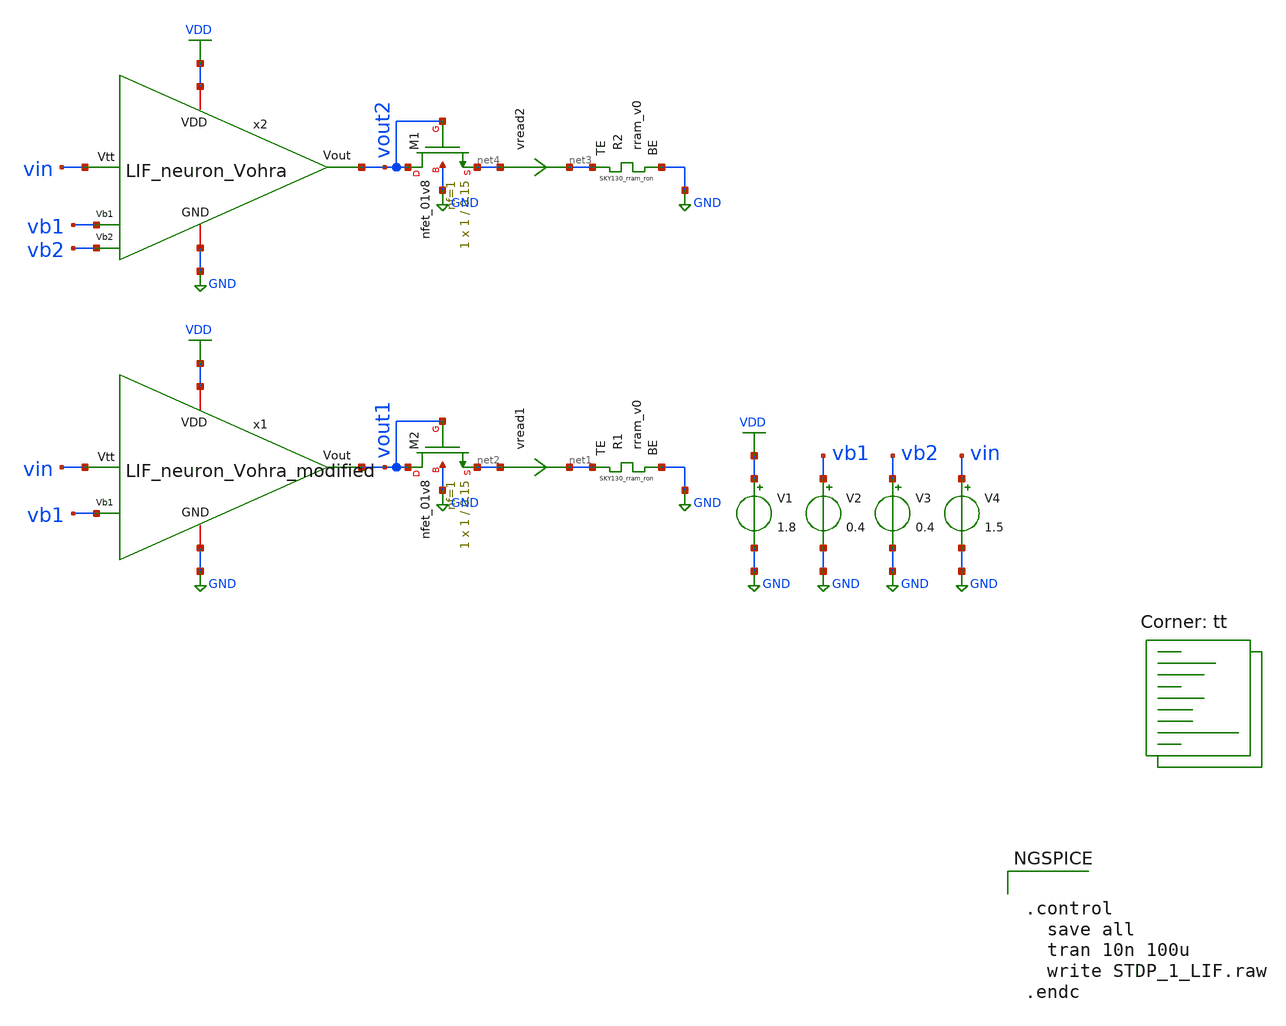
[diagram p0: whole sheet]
** sch_path: STDP/STDP_1_LIF_modified.sch
**.subckt STDP_1_LIF_modified
V1 VDD GND 1.8
V4 vin GND 1.5
V2 vb1 GND 0.4
XR1 net1 GND rram_v0
vread1 net2 net1 0
.save i(vread1)
x1 VDD vout1 vb1 GND vin LIF_neuron_Vohra_modified
x2 VDD vout2 vb1 vin GND vb2 LIF_neuron_Vohra
V3 vb2 GND 0.4
XR2 net3 GND rram_v0
vread2 net4 net3 0
.save i(vread2)
XM1 vout2 vout2 net4 GND sky130_fd_pr__nfet_01v8 L=0.15 W=1 nf=1 ad='int((nf+1)/2) * W/nf * 0.29' as='int((nf+2)/2) * W/nf * 0.29'
+ pd='2*int((nf+1)/2) * (W/nf + 0.29)' ps='2*int((nf+2)/2) * (W/nf + 0.29)' nrd='0.29 / W' nrs='0.29 / W'
+ sa=0 sb=0 sd=0 mult=1 m=1
XM2 vout1 vout1 net2 GND sky130_fd_pr__nfet_01v8 L=0.15 W=1 nf=1 ad='int((nf+1)/2) * W/nf * 0.29' as='int((nf+2)/2) * W/nf * 0.29'
+ pd='2*int((nf+1)/2) * (W/nf + 0.29)' ps='2*int((nf+2)/2) * (W/nf + 0.29)' nrd='0.29 / W' nrs='0.29 / W'
+ sa=0 sb=0 sd=0 mult=1 m=1
**** begin user architecture code
.lib $::SKYWATER_MODELS/sky130.lib.spice tt

** opencircuitdesign pdks install
.inc $::SKYWATER_MODELS/rram_v0.spice



.control
  save all
  tran 10n 100u
  write STDP_1_LIF.raw
.endc


**** end user architecture code
**.ends

* expanding   symbol:
*+  /home/ricardo/RATT_repos/Proyectos_xschem/LIF_neuron/LIF_neuron_Vohra_modified.sym # of pins=5
** sym_path: LIF_neuron/LIF_neuron_Vohra_modified.sym
** sch_path: LIF_neuron/LIF_neuron_Vohra_modified.sch
.subckt LIF_neuron_Vohra_modified VDD Vout Vb1 GND Vtt
*.ipin Vtt
*.iopin GND
*.ipin Vb1
*.iopin VDD
*.opin Vout
XM1 net2 Vtt GND GND sky130_fd_pr__nfet_01v8 L=1 W=0.6 nf=1 ad='int((nf+1)/2) * W/nf * 0.29' as='int((nf+2)/2) * W/nf * 0.29'
+ pd='2*int((nf+1)/2) * (W/nf + 0.29)' ps='2*int((nf+2)/2) * (W/nf + 0.29)' nrd='0.29 / W' nrs='0.29 / W'
+ sa=0 sb=0 sd=0 mult=1 m=1
XM3 net2 net2 VDD VDD sky130_fd_pr__pfet_01v8 L=1 W=0.6 nf=1 ad='int((nf+1)/2) * W/nf * 0.29' as='int((nf+2)/2) * W/nf * 0.29'
+ pd='2*int((nf+1)/2) * (W/nf + 0.29)' ps='2*int((nf+2)/2) * (W/nf + 0.29)' nrd='0.29 / W' nrs='0.29 / W'
+ sa=0 sb=0 sd=0 mult=1 m=1
XM13 net4 Vb1 GND GND sky130_fd_pr__nfet_01v8 L=0.5 W=5 nf=1 ad='int((nf+1)/2) * W/nf * 0.29' as='int((nf+2)/2) * W/nf * 0.29'
+ pd='2*int((nf+1)/2) * (W/nf + 0.29)' ps='2*int((nf+2)/2) * (W/nf + 0.29)' nrd='0.29 / W' nrs='0.29 / W'
+ sa=0 sb=0 sd=0 mult=1 m=1
XM12 rc net1 net5 GND sky130_fd_pr__nfet_01v8 L=1 W=1 nf=1 ad='int((nf+1)/2) * W/nf * 0.29' as='int((nf+2)/2) * W/nf * 0.29'
+ pd='2*int((nf+1)/2) * (W/nf + 0.29)' ps='2*int((nf+2)/2) * (W/nf + 0.29)' nrd='0.29 / W' nrs='0.29 / W'
+ sa=0 sb=0 sd=0 mult=1 m=1
XM11 rc net1 VDD VDD sky130_fd_pr__pfet_01v8 L=1 W=1 nf=1 ad='int((nf+1)/2) * W/nf * 0.29' as='int((nf+2)/2) * W/nf * 0.29'
+ pd='2*int((nf+1)/2) * (W/nf + 0.29)' ps='2*int((nf+2)/2) * (W/nf + 0.29)' nrd='0.29 / W' nrs='0.29 / W'
+ sa=0 sb=0 sd=0 mult=1 m=1
XC1 rc GND sky130_fd_pr__cap_mim_m3_1 W=21 L=1 MF=1 m=1
XM14 u rc GND GND sky130_fd_pr__nfet_01v8 L=4 W=1 nf=1 ad='int((nf+1)/2) * W/nf * 0.29' as='int((nf+2)/2) * W/nf * 0.29'
+ pd='2*int((nf+1)/2) * (W/nf + 0.29)' ps='2*int((nf+2)/2) * (W/nf + 0.29)' nrd='0.29 / W' nrs='0.29 / W'
+ sa=0 sb=0 sd=0 mult=1 m=1
XM4 u net2 VDD VDD sky130_fd_pr__pfet_01v8 L=1 W=1 nf=1 ad='int((nf+1)/2) * W/nf * 0.29' as='int((nf+2)/2) * W/nf * 0.29'
+ pd='2*int((nf+1)/2) * (W/nf + 0.29)' ps='2*int((nf+2)/2) * (W/nf + 0.29)' nrd='0.29 / W' nrs='0.29 / W'
+ sa=0 sb=0 sd=0 mult=1 m=1
XC2 u GND sky130_fd_pr__cap_mim_m3_1 W=10 L=1 MF=50 m=50
XM6 net3 Vout GND GND sky130_fd_pr__nfet_01v8 L=0.5 W=1 nf=1 ad='int((nf+1)/2) * W/nf * 0.29' as='int((nf+2)/2) * W/nf * 0.29'
+ pd='2*int((nf+1)/2) * (W/nf + 0.29)' ps='2*int((nf+2)/2) * (W/nf + 0.29)' nrd='0.29 / W' nrs='0.29 / W'
+ sa=0 sb=0 sd=0 mult=1 m=1
XM7 net1 u net3 GND sky130_fd_pr__nfet_01v8 L=1 W=1 nf=1 ad='int((nf+1)/2) * W/nf * 0.29' as='int((nf+2)/2) * W/nf * 0.29'
+ pd='2*int((nf+1)/2) * (W/nf + 0.29)' ps='2*int((nf+2)/2) * (W/nf + 0.29)' nrd='0.29 / W' nrs='0.29 / W'
+ sa=0 sb=0 sd=0 mult=1 m=1
XM8 net1 u VDD VDD sky130_fd_pr__pfet_01v8 L=1 W=1 nf=1 ad='int((nf+1)/2) * W/nf * 0.29' as='int((nf+2)/2) * W/nf * 0.29'
+ pd='2*int((nf+1)/2) * (W/nf + 0.29)' ps='2*int((nf+2)/2) * (W/nf + 0.29)' nrd='0.29 / W' nrs='0.29 / W'
+ sa=0 sb=0 sd=0 mult=1 m=1
XM9 Vout net1 net3 GND sky130_fd_pr__nfet_01v8 L=1 W=1 nf=1 ad='int((nf+1)/2) * W/nf * 0.29' as='int((nf+2)/2) * W/nf * 0.29'
+ pd='2*int((nf+1)/2) * (W/nf + 0.29)' ps='2*int((nf+2)/2) * (W/nf + 0.29)' nrd='0.29 / W' nrs='0.29 / W'
+ sa=0 sb=0 sd=0 mult=1 m=1
XM10 Vout net1 VDD VDD sky130_fd_pr__pfet_01v8 L=1 W=5 nf=1 ad='int((nf+1)/2) * W/nf * 0.29' as='int((nf+2)/2) * W/nf * 0.29'
+ pd='2*int((nf+1)/2) * (W/nf + 0.29)' ps='2*int((nf+2)/2) * (W/nf + 0.29)' nrd='0.29 / W' nrs='0.29 / W'
+ sa=0 sb=0 sd=0 mult=1 m=1
vread3 net5 net4 1e-4
.ends


* expanding   symbol:  /home/ricardo/RATT_repos/Proyectos_xschem/LIF_neuron/LIF_neuron_Vohra.sym #
*+ of pins=6
** sym_path: LIF_neuron/LIF_neuron_Vohra.sym
** sch_path: LIF_neuron/LIF_neuron_Vohra.sch
.subckt LIF_neuron_Vohra VDD Vout Vb1 Vtt GND Vb2
*.ipin Vtt
*.iopin GND
*.ipin Vb1
*.ipin Vb2
*.iopin VDD
*.opin Vout
XM1 net4 Vtt GND GND sky130_fd_pr__nfet_01v8 L=1 W=0.6 nf=1 ad='int((nf+1)/2) * W/nf * 0.29' as='int((nf+2)/2) * W/nf * 0.29'
+ pd='2*int((nf+1)/2) * (W/nf + 0.29)' ps='2*int((nf+2)/2) * (W/nf + 0.29)' nrd='0.29 / W' nrs='0.29 / W'
+ sa=0 sb=0 sd=0 mult=1 m=1
XM3 net4 net4 VDD VDD sky130_fd_pr__pfet_01v8 L=1 W=0.6 nf=1 ad='int((nf+1)/2) * W/nf * 0.29' as='int((nf+2)/2) * W/nf * 0.29'
+ pd='2*int((nf+1)/2) * (W/nf + 0.29)' ps='2*int((nf+2)/2) * (W/nf + 0.29)' nrd='0.29 / W' nrs='0.29 / W'
+ sa=0 sb=0 sd=0 mult=1 m=1
XM13 net3 Vb1 GND GND sky130_fd_pr__nfet_01v8 L=0.5 W=5 nf=1 ad='int((nf+1)/2) * W/nf * 0.29' as='int((nf+2)/2) * W/nf * 0.29'
+ pd='2*int((nf+1)/2) * (W/nf + 0.29)' ps='2*int((nf+2)/2) * (W/nf + 0.29)' nrd='0.29 / W' nrs='0.29 / W'
+ sa=0 sb=0 sd=0 mult=1 m=1
XM12 net1 net2 net3 GND sky130_fd_pr__nfet_01v8 L=1 W=1 nf=1 ad='int((nf+1)/2) * W/nf * 0.29' as='int((nf+2)/2) * W/nf * 0.29'
+ pd='2*int((nf+1)/2) * (W/nf + 0.29)' ps='2*int((nf+2)/2) * (W/nf + 0.29)' nrd='0.29 / W' nrs='0.29 / W'
+ sa=0 sb=0 sd=0 mult=1 m=1
XM11 net1 net2 VDD VDD sky130_fd_pr__pfet_01v8 L=1 W=1 nf=1 ad='int((nf+1)/2) * W/nf * 0.29' as='int((nf+2)/2) * W/nf * 0.29'
+ pd='2*int((nf+1)/2) * (W/nf + 0.29)' ps='2*int((nf+2)/2) * (W/nf + 0.29)' nrd='0.29 / W' nrs='0.29 / W'
+ sa=0 sb=0 sd=0 mult=1 m=1
XC1 net1 GND sky130_fd_pr__cap_mim_m3_1 W=21 L=1 MF=1 m=1
XM14 net5 net1 GND GND sky130_fd_pr__nfet_01v8 L=1 W=1 nf=1 ad='int((nf+1)/2) * W/nf * 0.29' as='int((nf+2)/2) * W/nf * 0.29'
+ pd='2*int((nf+1)/2) * (W/nf + 0.29)' ps='2*int((nf+2)/2) * (W/nf + 0.29)' nrd='0.29 / W' nrs='0.29 / W'
+ sa=0 sb=0 sd=0 mult=1 m=1
XM4 net5 net4 VDD VDD sky130_fd_pr__pfet_01v8 L=1 W=1 nf=1 ad='int((nf+1)/2) * W/nf * 0.29' as='int((nf+2)/2) * W/nf * 0.29'
+ pd='2*int((nf+1)/2) * (W/nf + 0.29)' ps='2*int((nf+2)/2) * (W/nf + 0.29)' nrd='0.29 / W' nrs='0.29 / W'
+ sa=0 sb=0 sd=0 mult=1 m=1
XC2 net5 GND sky130_fd_pr__cap_mim_m3_1 W=10 L=1 MF=50 m=50
XM5 net5 Vb2 GND GND sky130_fd_pr__nfet_01v8 L=1 W=2 nf=1 ad='int((nf+1)/2) * W/nf * 0.29' as='int((nf+2)/2) * W/nf * 0.29'
+ pd='2*int((nf+1)/2) * (W/nf + 0.29)' ps='2*int((nf+2)/2) * (W/nf + 0.29)' nrd='0.29 / W' nrs='0.29 / W'
+ sa=0 sb=0 sd=0 mult=1 m=1
XM6 net6 Vout GND GND sky130_fd_pr__nfet_01v8 L=1 W=1 nf=1 ad='int((nf+1)/2) * W/nf * 0.29' as='int((nf+2)/2) * W/nf * 0.29'
+ pd='2*int((nf+1)/2) * (W/nf + 0.29)' ps='2*int((nf+2)/2) * (W/nf + 0.29)' nrd='0.29 / W' nrs='0.29 / W'
+ sa=0 sb=0 sd=0 mult=1 m=1
XM7 net2 net5 net6 GND sky130_fd_pr__nfet_01v8 L=1 W=1 nf=1 ad='int((nf+1)/2) * W/nf * 0.29' as='int((nf+2)/2) * W/nf * 0.29'
+ pd='2*int((nf+1)/2) * (W/nf + 0.29)' ps='2*int((nf+2)/2) * (W/nf + 0.29)' nrd='0.29 / W' nrs='0.29 / W'
+ sa=0 sb=0 sd=0 mult=1 m=1
XM8 net2 net5 VDD VDD sky130_fd_pr__pfet_01v8 L=1 W=1 nf=1 ad='int((nf+1)/2) * W/nf * 0.29' as='int((nf+2)/2) * W/nf * 0.29'
+ pd='2*int((nf+1)/2) * (W/nf + 0.29)' ps='2*int((nf+2)/2) * (W/nf + 0.29)' nrd='0.29 / W' nrs='0.29 / W'
+ sa=0 sb=0 sd=0 mult=1 m=1
XM9 Vout net2 net6 GND sky130_fd_pr__nfet_01v8 L=1 W=1 nf=1 ad='int((nf+1)/2) * W/nf * 0.29' as='int((nf+2)/2) * W/nf * 0.29'
+ pd='2*int((nf+1)/2) * (W/nf + 0.29)' ps='2*int((nf+2)/2) * (W/nf + 0.29)' nrd='0.29 / W' nrs='0.29 / W'
+ sa=0 sb=0 sd=0 mult=1 m=1
XM10 Vout net2 VDD VDD sky130_fd_pr__pfet_01v8 L=1 W=5 nf=1 ad='int((nf+1)/2) * W/nf * 0.29' as='int((nf+2)/2) * W/nf * 0.29'
+ pd='2*int((nf+1)/2) * (W/nf + 0.29)' ps='2*int((nf+2)/2) * (W/nf + 0.29)' nrd='0.29 / W' nrs='0.29 / W'
+ sa=0 sb=0 sd=0 mult=1 m=1
.ends

.GLOBAL GND
.GLOBAL VDD
.end
